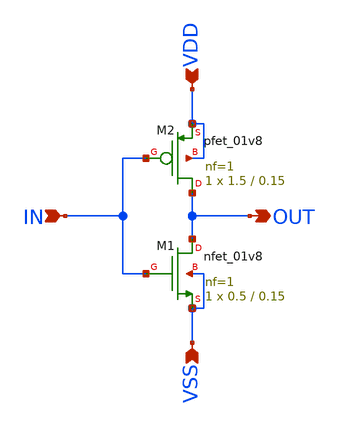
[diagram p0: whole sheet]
** sch_path: files/Analog_Inverter/2_layout/Reference_Inverter_using_sky130A/inverter_example.sch
**.subckt inverter_example IN VDD VSS OUT
*.ipin IN
*.ipin VDD
*.ipin VSS
*.opin OUT
XM1 OUT IN VSS VSS sky130_fd_pr__nfet_01v8 L=0.15 W=0.5 nf=1 ad='int((nf+1)/2) * W/nf * 0.29' as='int((nf+2)/2) * W/nf * 0.29'
+ pd='2*int((nf+1)/2) * (W/nf + 0.29)' ps='2*int((nf+2)/2) * (W/nf + 0.29)' nrd='0.29 / W' nrs='0.29 / W'
+ sa=0 sb=0 sd=0 mult=1 m=1
XM2 OUT IN VDD VDD sky130_fd_pr__pfet_01v8 L=0.15 W=1.5 nf=1 ad='int((nf+1)/2) * W/nf * 0.29' as='int((nf+2)/2) * W/nf * 0.29'
+ pd='2*int((nf+1)/2) * (W/nf + 0.29)' ps='2*int((nf+2)/2) * (W/nf + 0.29)' nrd='0.29 / W' nrs='0.29 / W'
+ sa=0 sb=0 sd=0 mult=1 m=1
**.ends
.end
